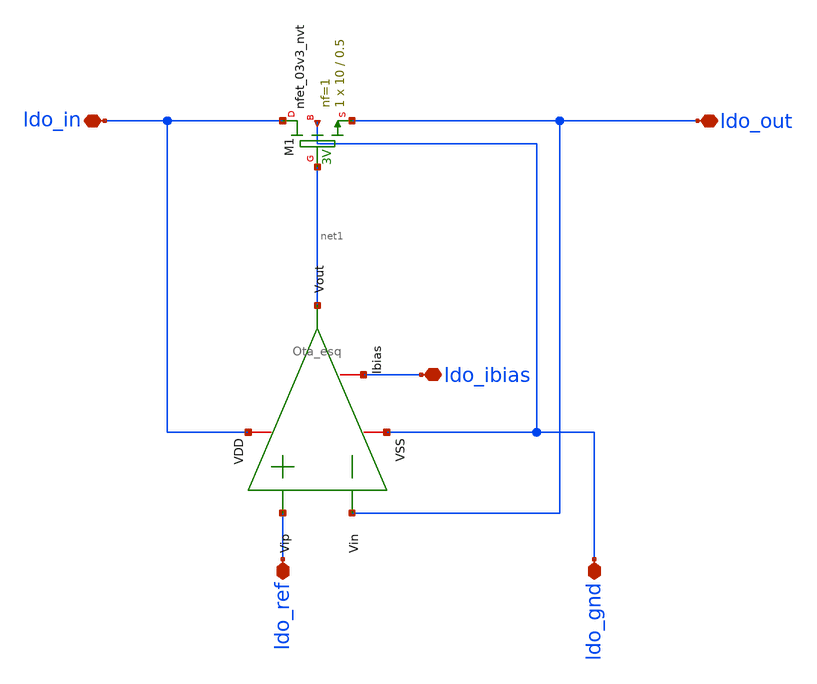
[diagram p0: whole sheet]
** sch_path: xschem/LDO.sch
**.subckt LDO ldo_out ldo_in ldo_gnd ldo_ref ldo_ibias
*.iopin ldo_out
*.iopin ldo_in
*.iopin ldo_gnd
*.iopin ldo_ref
*.iopin ldo_ibias
x1 ldo_in ldo_out ldo_ref net1 ldo_ibias ldo_gnd Ota_esq
XM1 ldo_in net1 ldo_out ldo_gnd sky130_fd_pr__nfet_03v3_nvt L=0.5 W=10 nf=1 ad='int((nf+1)/2) * W/nf * 0.29'
+ as='int((nf+2)/2) * W/nf * 0.29' pd='2*int((nf+1)/2) * (W/nf + 0.29)' ps='2*int((nf+2)/2) * (W/nf + 0.29)'
+ nrd='0.29 / W' nrs='0.29 / W' sa=0 sb=0 sd=0 mult=1 m=1
**.ends

* expanding   symbol:  Ota_esq.sym # of pins=6
** sym_path: xschem/Ota_esq.sym
** sch_path: xschem/Ota_esq.sch
.subckt Ota_esq VDD Vin Vip Vout Ibias VSS
*.ipin Vin
*.ipin Vip
*.iopin VDD
*.iopin VSS
*.iopin Ibias
*.opin Vout
XC1 net2 Vout sky130_fd_pr__cap_mim_m3_1 W=23 L=23 MF=1 m=1
XM3 VSS net1 net1 VSS sky130_fd_pr__nfet_g5v0d10v5 L=0.5 W=7 nf=1 ad='int((nf+1)/2) * W/nf * 0.29' as='int((nf+2)/2) * W/nf * 0.29'
+ pd='2*int((nf+1)/2) * (W/nf + 0.29)' ps='2*int((nf+2)/2) * (W/nf + 0.29)' nrd='0.29 / W' nrs='0.29 / W'
+ sa=0 sb=0 sd=0 mult=1 m=1
XM1 net1 Vin net3 net3 sky130_fd_pr__pfet_g5v0d10v5 L=0.5 W=2 nf=1 ad='int((nf+1)/2) * W/nf * 0.29' as='int((nf+2)/2) * W/nf * 0.29'
+ pd='2*int((nf+1)/2) * (W/nf + 0.29)' ps='2*int((nf+2)/2) * (W/nf + 0.29)' nrd='0.29 / W' nrs='0.29 / W'
+ sa=0 sb=0 sd=0 mult=1 m=1
XM2 net3 Vip net2 net3 sky130_fd_pr__pfet_g5v0d10v5 L=0.5 W=2 nf=1 ad='int((nf+1)/2) * W/nf * 0.29' as='int((nf+2)/2) * W/nf * 0.29'
+ pd='2*int((nf+1)/2) * (W/nf + 0.29)' ps='2*int((nf+2)/2) * (W/nf + 0.29)' nrd='0.29 / W' nrs='0.29 / W'
+ sa=0 sb=0 sd=0 mult=1 m=1
XM4 net2 net1 VSS VSS sky130_fd_pr__nfet_g5v0d10v5 L=0.5 W=7 nf=1 ad='int((nf+1)/2) * W/nf * 0.29' as='int((nf+2)/2) * W/nf * 0.29'
+ pd='2*int((nf+1)/2) * (W/nf + 0.29)' ps='2*int((nf+2)/2) * (W/nf + 0.29)' nrd='0.29 / W' nrs='0.29 / W'
+ sa=0 sb=0 sd=0 mult=1 m=1
XM7 Vout net2 VSS VSS sky130_fd_pr__nfet_g5v0d10v5 L=1 W=21 nf=7 ad='int((nf+1)/2) * W/nf * 0.29' as='int((nf+2)/2) * W/nf * 0.29'
+ pd='2*int((nf+1)/2) * (W/nf + 0.29)' ps='2*int((nf+2)/2) * (W/nf + 0.29)' nrd='0.29 / W' nrs='0.29 / W'
+ sa=0 sb=0 sd=0 mult=1 m=1
XM8 VDD Ibias Ibias VDD sky130_fd_pr__pfet_g5v0d10v5 L=1 W=24 nf=8 ad='int((nf+1)/2) * W/nf * 0.29' as='int((nf+2)/2) * W/nf * 0.29'
+ pd='2*int((nf+1)/2) * (W/nf + 0.29)' ps='2*int((nf+2)/2) * (W/nf + 0.29)' nrd='0.29 / W' nrs='0.29 / W'
+ sa=0 sb=0 sd=0 mult=1 m=1
XM5 net3 Ibias VDD VDD sky130_fd_pr__pfet_g5v0d10v5 L=1 W=24 nf=8 ad='int((nf+1)/2) * W/nf * 0.29' as='int((nf+2)/2) * W/nf * 0.29'
+ pd='2*int((nf+1)/2) * (W/nf + 0.29)' ps='2*int((nf+2)/2) * (W/nf + 0.29)' nrd='0.29 / W' nrs='0.29 / W'
+ sa=0 sb=0 sd=0 mult=1 m=1
XM6 Vout Ibias VDD VDD sky130_fd_pr__pfet_g5v0d10v5 L=1 W=39 nf=13 ad='int((nf+1)/2) * W/nf * 0.29' as='int((nf+2)/2) * W/nf * 0.29'
+ pd='2*int((nf+1)/2) * (W/nf + 0.29)' ps='2*int((nf+2)/2) * (W/nf + 0.29)' nrd='0.29 / W' nrs='0.29 / W'
+ sa=0 sb=0 sd=0 mult=1 m=1
.ends

.end
